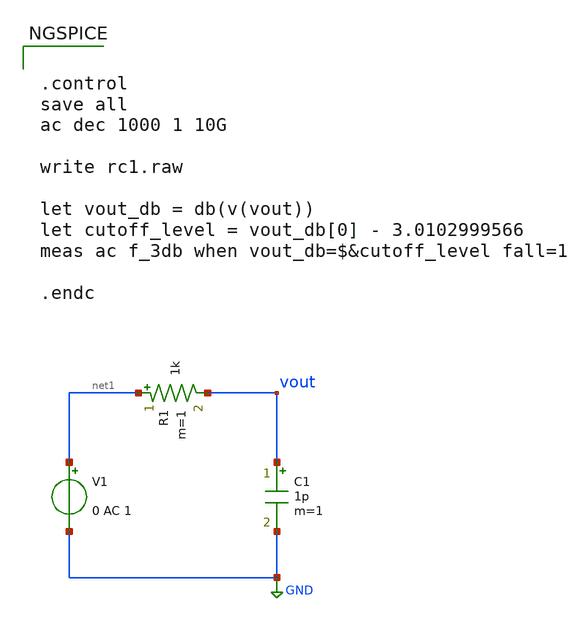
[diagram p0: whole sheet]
** sch_path: 20260805_poles_to_rc_circuit/rc1.sch
**.subckt rc1
R1 net1 vout 1k m=1
C1 vout GND 1p m=1
V1 net1 GND 0 AC 1
**** begin user architecture code


.control
save all
ac dec 1000 1 10G

write rc1.raw

let vout_db = db(v(vout))
let cutoff_level = vout_db[0] - 3.0102999566
meas ac f_3db when vout_db=$&cutoff_level fall=1

.endc


**** end user architecture code
**.ends
.GLOBAL GND
.end
